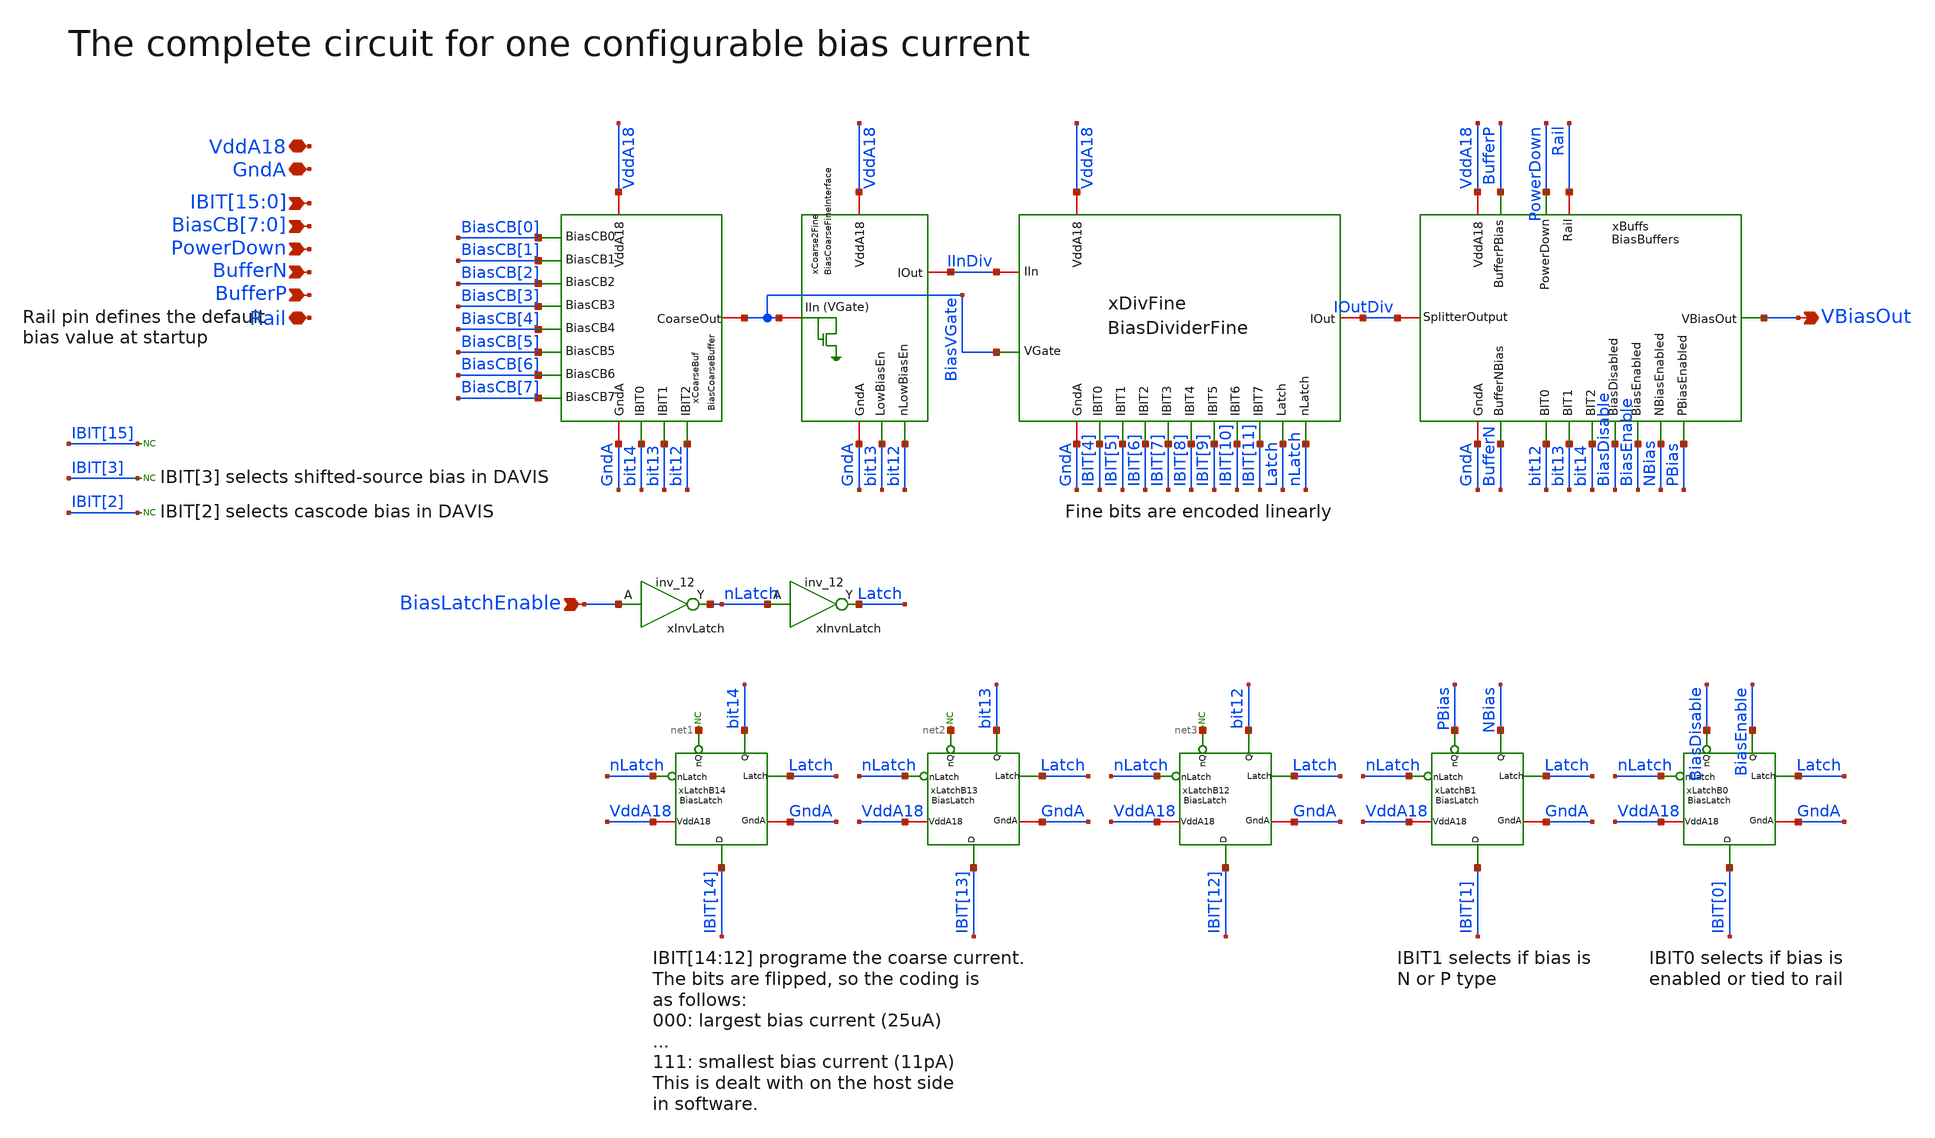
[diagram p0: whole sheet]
** sch_path: analog/xschem/BiasBranch.sch
**.subckt BiasBranch VddA18 GndA VBiasOut BiasLatchEnable
*+ IBIT[15],IBIT[14],IBIT[13],IBIT[12],IBIT[11],IBIT[10],IBIT[9],IBIT[8],IBIT[7],IBIT[6],IBIT[5],IBIT[4],IBIT[3],IBIT[2],IBIT[1],IBIT[0] BiasCB[7],BiasCB[6],BiasCB[5],BiasCB[4],BiasCB[3],BiasCB[2],BiasCB[1],BiasCB[0] PowerDown BufferN
*+ BufferP Rail
*.iopin VddA18
*.iopin GndA
*.opin VBiasOut
*.ipin BiasLatchEnable
*.ipin
*+ IBIT[15],IBIT[14],IBIT[13],IBIT[12],IBIT[11],IBIT[10],IBIT[9],IBIT[8],IBIT[7],IBIT[6],IBIT[5],IBIT[4],IBIT[3],IBIT[2],IBIT[1],IBIT[0]
*.ipin BiasCB[7],BiasCB[6],BiasCB[5],BiasCB[4],BiasCB[3],BiasCB[2],BiasCB[1],BiasCB[0]
*.ipin PowerDown
*.ipin BufferN
*.ipin BufferP
*.iopin Rail
xCoarseBuf VddA18 GndA bit14 bit13 bit12 BiasVGate BiasCB[0] BiasCB[1] BiasCB[3] BiasCB[4] BiasCB[5]
+ BiasCB[6] BiasCB[7] BiasCB[2] BiasCoarseBuffer
xCoarse2Fine VddA18 GndA bit13 bit12 BiasVGate IInDiv BiasCoarseFineInterface
xDivFine VddA18 GndA IBIT[4] IBIT[5] IInDiv IOutDiv IBIT[6] IBIT[7] IBIT[8] IBIT[9] IBIT[10]
+ IBIT[11] Latch nLatch BiasVGate BiasDividerFine
xBuffs VddA18 GndA BufferN IOutDiv bit12 bit13 bit14 BiasDisable BiasEnable NBias PBias BufferP
+ PowerDown Rail VBiasOut BiasBuffers
xInvLatch BiasLatchEnable GndA GndA VddA18 VddA18 nLatch sky130_fd_sc_hd__inv_12
xInvnLatch nLatch GndA GndA VddA18 VddA18 Latch sky130_fd_sc_hd__inv_12
xLatchB14 VddA18 GndA net1 bit14 Latch nLatch IBIT[14] BiasLatch
* noconn #net1
xLatchB13 VddA18 GndA net2 bit13 Latch nLatch IBIT[13] BiasLatch
* noconn #net2
xLatchB12 VddA18 GndA net3 bit12 Latch nLatch IBIT[12] BiasLatch
* noconn #net3
xLatchB1 VddA18 GndA PBias NBias Latch nLatch IBIT[1] BiasLatch
xLatchB0 VddA18 GndA BiasDisable BiasEnable Latch nLatch IBIT[0] BiasLatch
* noconn IBIT[15]
* noconn IBIT[3]
* noconn IBIT[2]
**.ends
.end
